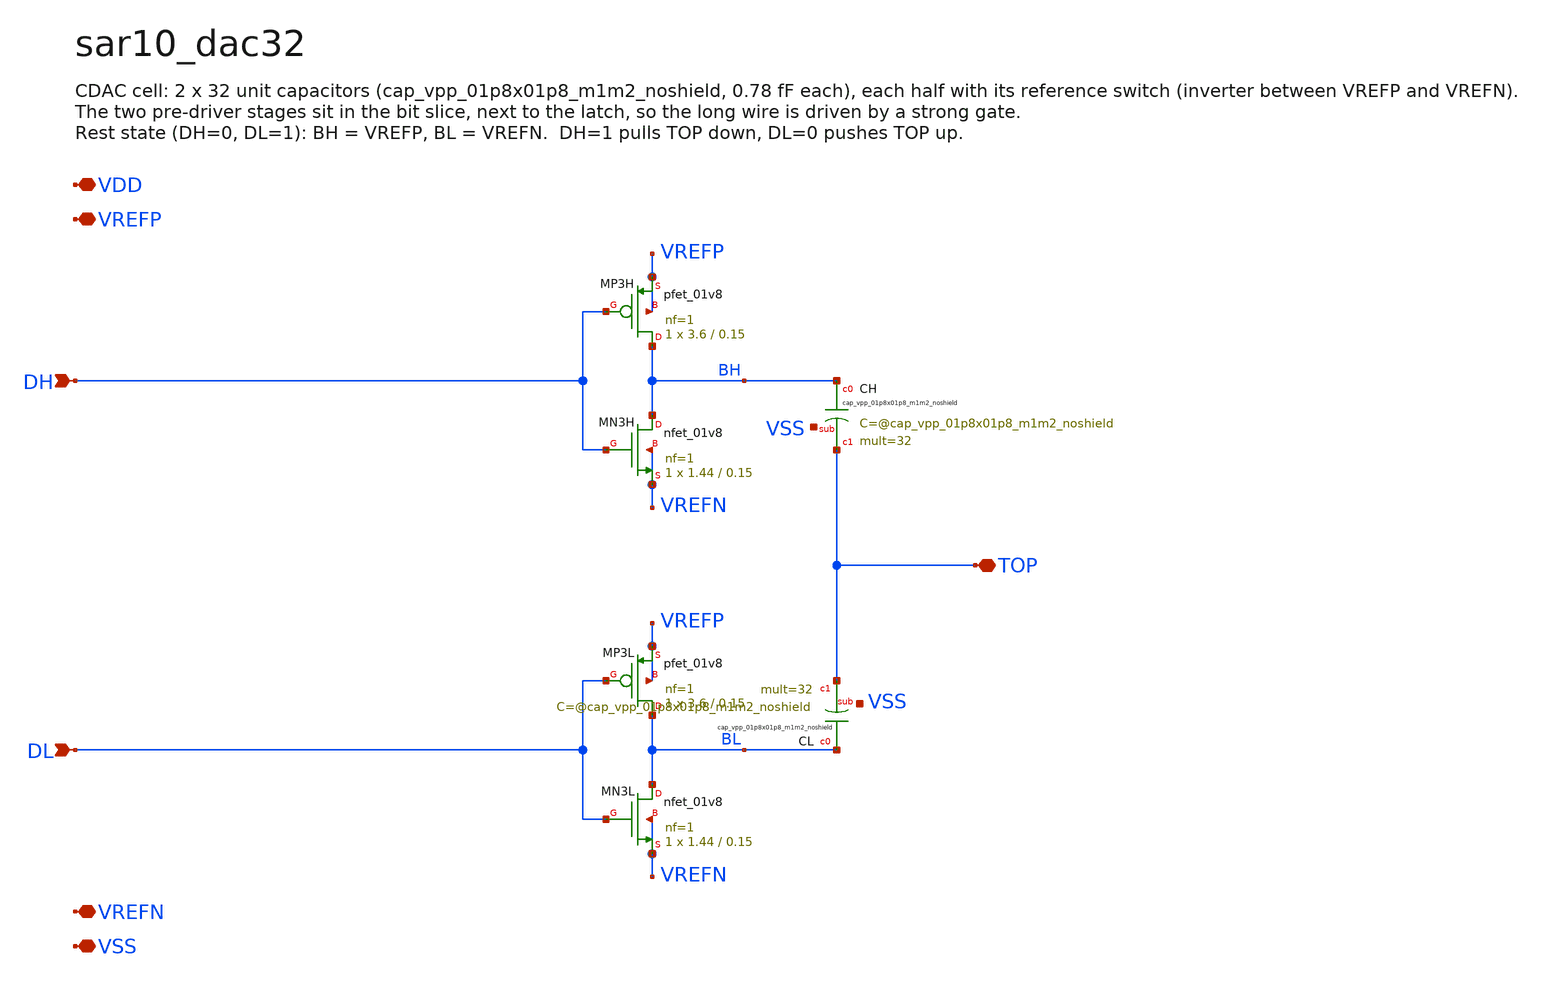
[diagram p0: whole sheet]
** sch_path: xschem/sar10_dac32.sch
**.subckt sar10_dac32 DH DL TOP VDD VREFP VREFN VSS
*.ipin DH
*.ipin DL
*.iopin TOP
*.iopin VDD
*.iopin VREFP
*.iopin VREFN
*.iopin VSS
XMP3H BH DH VREFP VREFP sky130_fd_pr__pfet_01v8 L=0.15 W=3.6 nf=1 ad='int((1 + 1)/2) * 3.6 / 1 * 0.29'
+ as='int((1 + 2)/2) * 3.6 / 1 * 0.29' pd='2*int((1 + 1)/2) * (3.6 / 1 + 0.29)' ps='2*int((1 + 2)/2) * (3.6 / 1 + 0.29)'
+ nrd='0.29 / 3.6 ' nrs='0.29 / 3.6 ' sa=0 sb=0 sd=0 mult=1 m=1
XMN3H BH DH VREFN VREFN sky130_fd_pr__nfet_01v8 L=0.15 W=1.44 nf=1 ad='int((1 + 1)/2) * 1.44 / 1 * 0.29'
+ as='int((1 + 2)/2) * 1.44 / 1 * 0.29' pd='2*int((1 + 1)/2) * (1.44 / 1 + 0.29)' ps='2*int((1 + 2)/2) * (1.44 / 1 + 0.29)'
+ nrd='0.29 / 1.44 ' nrs='0.29 / 1.44 ' sa=0 sb=0 sd=0 mult=1 m=1
XMP3L BL DL VREFP VREFP sky130_fd_pr__pfet_01v8 L=0.15 W=3.6 nf=1 ad='int((1 + 1)/2) * 3.6 / 1 * 0.29'
+ as='int((1 + 2)/2) * 3.6 / 1 * 0.29' pd='2*int((1 + 1)/2) * (3.6 / 1 + 0.29)' ps='2*int((1 + 2)/2) * (3.6 / 1 + 0.29)'
+ nrd='0.29 / 3.6 ' nrs='0.29 / 3.6 ' sa=0 sb=0 sd=0 mult=1 m=1
XMN3L BL DL VREFN VREFN sky130_fd_pr__nfet_01v8 L=0.15 W=1.44 nf=1 ad='int((1 + 1)/2) * 1.44 / 1 * 0.29'
+ as='int((1 + 2)/2) * 1.44 / 1 * 0.29' pd='2*int((1 + 1)/2) * (1.44 / 1 + 0.29)' ps='2*int((1 + 2)/2) * (1.44 / 1 + 0.29)'
+ nrd='0.29 / 1.44 ' nrs='0.29 / 1.44 ' sa=0 sb=0 sd=0 mult=1 m=1
XCH BH TOP VSS sky130_fd_pr__cap_vpp_01p8x01p8_m1m2_noshield mult=32 m=32
XCL BL TOP VSS sky130_fd_pr__cap_vpp_01p8x01p8_m1m2_noshield mult=32 m=32
**.ends
.end
